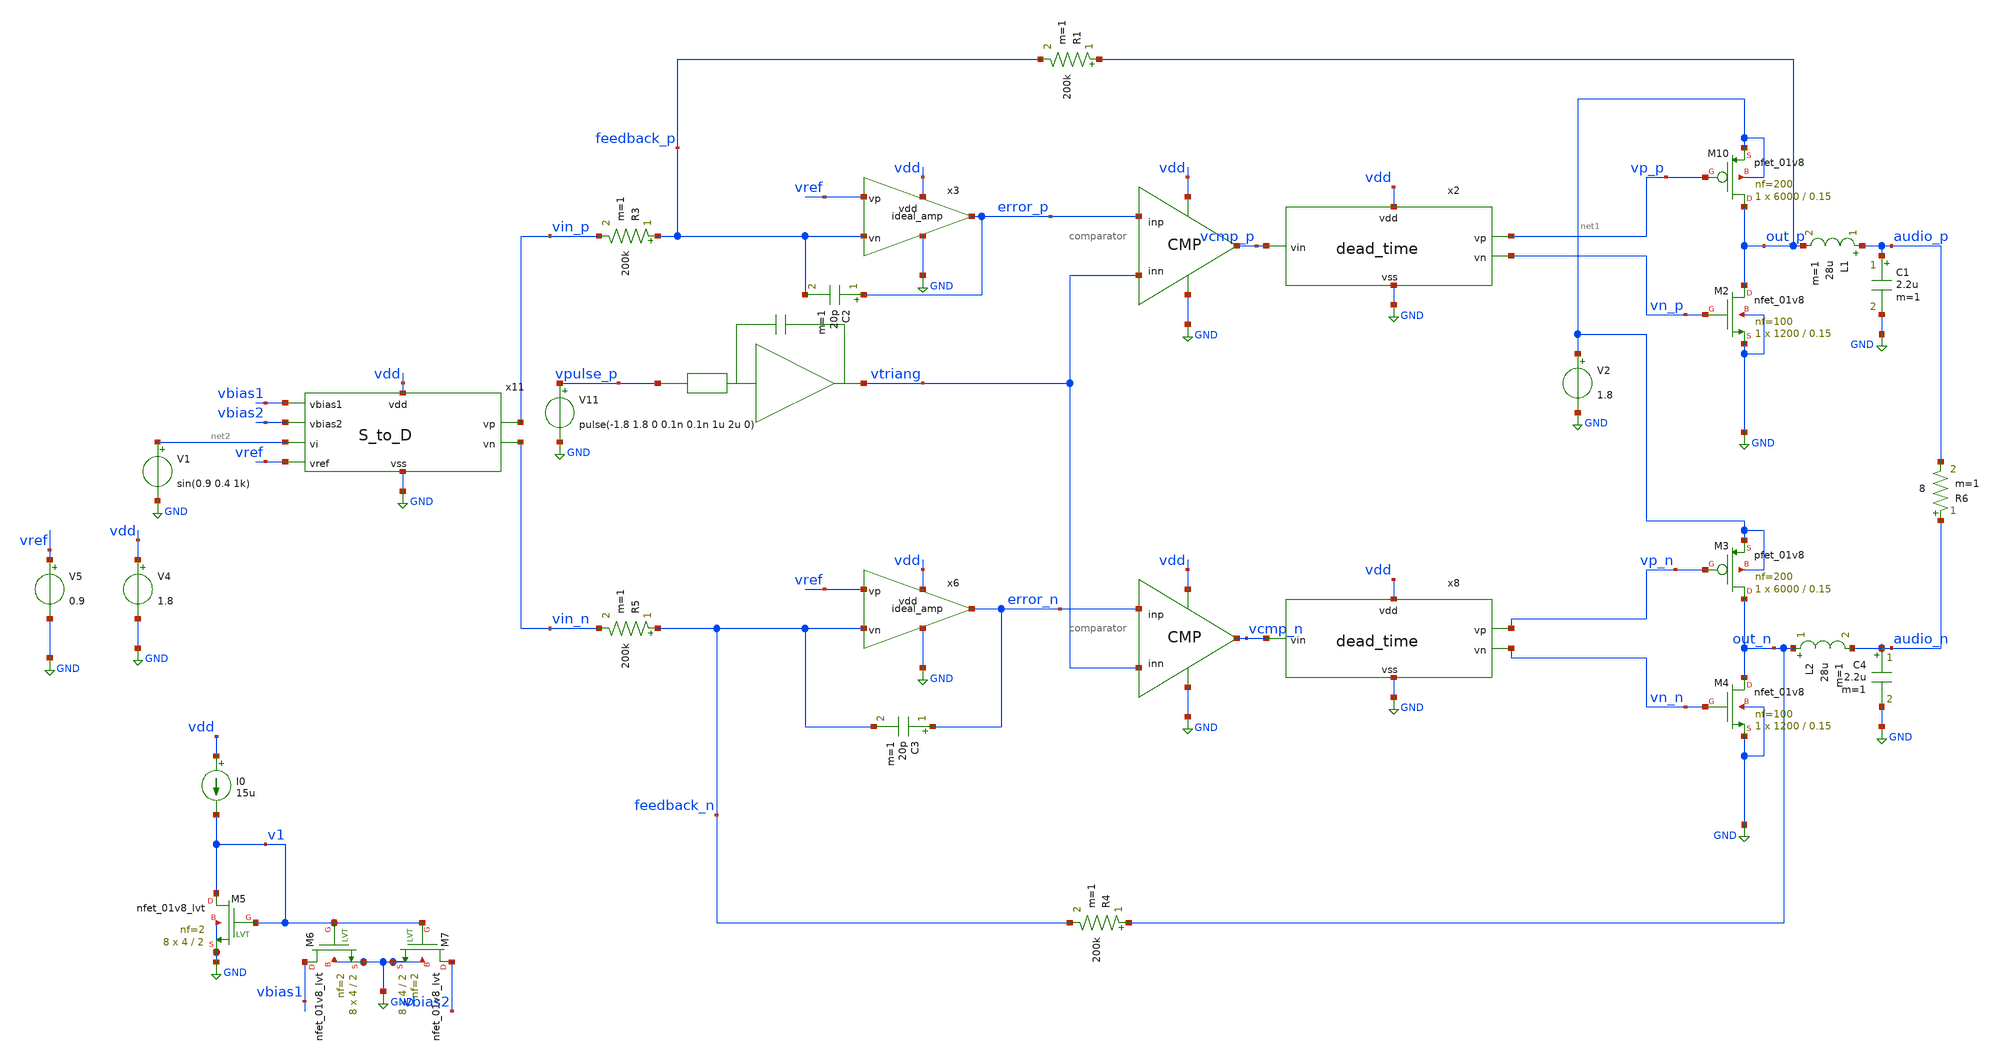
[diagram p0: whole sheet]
** sch_path: xschem/src/behavior_mdl/behavior_model_fine.sch
**.subckt behavior_model_fine
V1 net2 GND sin(0.9 0.4 1k)
x5 vpulse_p vtriang triang
V5 vref GND 0.9
x3 vref feedback_p error_p vdd GND ideal_amp
x1 error_p vtriang vcmp_p vdd GND comparator
L1 audio_p out_p 28u m=1
C1 audio_p GND 2.2u m=1
R1 out_p feedback_p 200k m=1
R3 feedback_p vin_p 200k m=1
C2 error_p feedback_p 20p m=1
x6 vref feedback_n error_n vdd GND ideal_amp
x7 error_n vtriang vcmp_n vdd GND comparator
R4 out_n feedback_n 200k m=1
R5 feedback_n vin_n 200k m=1
C3 error_n feedback_n 20p m=1
L2 out_n audio_n 28u m=1
C4 audio_n GND 2.2u m=1
R6 audio_n audio_p 8 m=1
V11 vpulse_p GND pulse(-1.8 1.8 0 0.1n 0.1n 1u 2u 0)
XM10 out_p vp_p net1 net1 sky130_fd_pr__pfet_01v8 L=0.15 W=6000 nf=200 ad='int((nf+1)/2) * W/nf * 0.29'
+ as='int((nf+2)/2) * W/nf * 0.29' pd='2*int((nf+1)/2) * (W/nf + 0.29)' ps='2*int((nf+2)/2) * (W/nf + 0.29)'
+ nrd='0.29 / W' nrs='0.29 / W' sa=0 sb=0 sd=0 mult=1 m=1
XM2 out_p vn_p GND GND sky130_fd_pr__nfet_01v8 L=0.15 W=1200 nf=100 ad='int((nf+1)/2) * W/nf * 0.29'
+ as='int((nf+2)/2) * W/nf * 0.29' pd='2*int((nf+1)/2) * (W/nf + 0.29)' ps='2*int((nf+2)/2) * (W/nf + 0.29)'
+ nrd='0.29 / W' nrs='0.29 / W' sa=0 sb=0 sd=0 mult=1 m=1
XM3 out_n vp_n net1 net1 sky130_fd_pr__pfet_01v8 L=0.15 W=6000 nf=200 ad='int((nf+1)/2) * W/nf * 0.29'
+ as='int((nf+2)/2) * W/nf * 0.29' pd='2*int((nf+1)/2) * (W/nf + 0.29)' ps='2*int((nf+2)/2) * (W/nf + 0.29)'
+ nrd='0.29 / W' nrs='0.29 / W' sa=0 sb=0 sd=0 mult=1 m=1
XM4 out_n vn_n GND GND sky130_fd_pr__nfet_01v8 L=0.15 W=1200 nf=100 ad='int((nf+1)/2) * W/nf * 0.29'
+ as='int((nf+2)/2) * W/nf * 0.29' pd='2*int((nf+1)/2) * (W/nf + 0.29)' ps='2*int((nf+2)/2) * (W/nf + 0.29)'
+ nrd='0.29 / W' nrs='0.29 / W' sa=0 sb=0 sd=0 mult=1 m=1
V4 vdd GND 1.8
x2 vdd vcmp_p vp_p vn_p GND dead_time
x8 vdd vcmp_n vp_n vn_n GND dead_time
x11 vdd vbias1 vbias2 net2 vref GND vin_n vin_p S_to_D
V2 net1 GND 1.8
I0 vdd v1 15u
XM5 v1 v1 GND GND sky130_fd_pr__nfet_01v8_lvt L=2 W=4 nf=2 ad='int((nf+1)/2) * W/nf * 0.29' as='int((nf+2)/2) * W/nf * 0.29'
+ pd='2*int((nf+1)/2) * (W/nf + 0.29)' ps='2*int((nf+2)/2) * (W/nf + 0.29)' nrd='0.29 / W' nrs='0.29 / W'
+ sa=0 sb=0 sd=0 mult=8 m=8
XM6 vbias1 v1 GND GND sky130_fd_pr__nfet_01v8_lvt L=2 W=4 nf=2 ad='int((nf+1)/2) * W/nf * 0.29' as='int((nf+2)/2) * W/nf * 0.29'
+ pd='2*int((nf+1)/2) * (W/nf + 0.29)' ps='2*int((nf+2)/2) * (W/nf + 0.29)' nrd='0.29 / W' nrs='0.29 / W'
+ sa=0 sb=0 sd=0 mult=8 m=8
XM7 vbias2 v1 GND GND sky130_fd_pr__nfet_01v8_lvt L=2 W=4 nf=2 ad='int((nf+1)/2) * W/nf * 0.29' as='int((nf+2)/2) * W/nf * 0.29'
+ pd='2*int((nf+1)/2) * (W/nf + 0.29)' ps='2*int((nf+2)/2) * (W/nf + 0.29)' nrd='0.29 / W' nrs='0.29 / W'
+ sa=0 sb=0 sd=0 mult=8 m=8
**** begin user architecture code


.include /home/eda/xschem/xschem_library/src/behavior_mdl/comparator.spice
.include /home/eda/xschem/xschem_library/src/behavior_mdl/switch.spice
*.include /home/eda/xschem/xschem_library/src/behavior_mdl/integrator_feedback.spice
*.include /home/eda/xschem/xschem_library/src/behavior_mdl/integrator_input.spice
*.include /home/eda/xschem/xschem_library/src/behavior_mdl/adder.spice
.include /home/eda/xschem/xschem_library/src/behavior_mdl/triang.spice
.include /home/eda/xschem/xschem_library/src/behavior_mdl/ideal_amp.spice
.include /home/eda/xschem/xschem_library/src/behavior_mdl/limiter.spice




.option VNTOL=1e-6 ABSTOL=5e-9
.nodeset v(vin_p)=0.9 v(vin_n)=0.9 v(out_p)=0.9 v(out_n)=0.9 v(error_p)=0.9 v(error_n)=0.9
*set the absolute voltage error tolerance and absolute current error tolerance
.control
save vtriang vin_p vin_n error_n error_p vcmp_n vcmp_p vp_p vn_p vp_n vn_n out_p out_n audio_p
+ audio_n feedback_p feedback_n I(V4) I(V2) @r6[i] @r1[i]
tran 1n 10m 1m
*op
*linearize V(audio)
*linearize V(out)
*fft V(out)
*fft V(audio)
*plot mag(V(audio))
*plot mag(V(out))
let pout=@r6[i]*(V(audio_p)-V(audio_n))
let pin=1.8*I(V2)
meas tran pload avg pout from=1m to=4m
meas tran p_supply avg pin from=1m to=4m
print pload/p_supply
set nfreqs=20
fourier 1k V(audio_p)-V(audio_n)
write behavior_1k_04.raw

.endc





.include /home/eda/pdk/skywater-pdk/libraries/sky130_fd_pr_ngspice/latest/models/corners/tt.spice
.include /home/eda/magic/class_d_audio_amplifier/OTA/OTA_int_post.spice
.include /home/eda/magic/class_d_audio_amplifier/OTA/OTA_post.spice
.include /home/eda/magic/class_d_audio_amplifier/S_to_D/S_to_D_post.spice
.include /home/eda/magic/class_d_audio_amplifier/triang/triangle_post.spice

* Resistor$::SKYWATER_MODELS/Capacitor
.include $::SKYWATER_MODELS/models/r+c/res_typical__cap_typical.spice
.include $::SKYWATER_MODELS/models/r+c/res_typical__cap_typical__lin.spice
* Special cells
.include $::SKYWATER_MODELS/models/corners/tt/specialized_cells.spice


**** end user architecture code
**.ends

* expanding   symbol:  src/dead_time/dead_time.sym # of pins=5
** sym_path: xschem/src/dead_time/dead_time.sym
** sch_path: xschem/src/dead_time/dead_time.sch
.subckt dead_time vdd vin vp vn vss
*.ipin vin
*.iopin vdd
*.opin vp
*.iopin vss
*.opin vn
x1 vdd vin vinn vss inverter
x2 vdd net1 vin net4 vss nand
x3 vdd net2 net3 vinn vss nand
XC1 net1 vss sky130_fd_pr__cap_mim_m3_1 W=17.75 L=17.75 MF=16 m=16
XM3 net5 net1 vss vss sky130_fd_pr__nfet_01v8 L=0.15 W=5 nf=2 ad='int((nf+1)/2) * W/nf * 0.29' as='int((nf+2)/2) * W/nf * 0.29'
+ pd='2*int((nf+1)/2) * (W/nf + 0.29)' ps='2*int((nf+2)/2) * (W/nf + 0.29)' nrd='0.29 / W' nrs='0.29 / W'
+ sa=0 sb=0 sd=0 mult=1 m=1
XM1 net5 net1 vdd vdd sky130_fd_pr__pfet_01v8 L=0.15 W=10 nf=2 ad='int((nf+1)/2) * W/nf * 0.29' as='int((nf+2)/2) * W/nf * 0.29'
+ pd='2*int((nf+1)/2) * (W/nf + 0.29)' ps='2*int((nf+2)/2) * (W/nf + 0.29)' nrd='0.29 / W' nrs='0.29 / W'
+ sa=0 sb=0 sd=0 mult=1 m=1
XM2 net3 net5 vss vss sky130_fd_pr__nfet_01v8 L=0.15 W=20 nf=8 ad='int((nf+1)/2) * W/nf * 0.29' as='int((nf+2)/2) * W/nf * 0.29'
+ pd='2*int((nf+1)/2) * (W/nf + 0.29)' ps='2*int((nf+2)/2) * (W/nf + 0.29)' nrd='0.29 / W' nrs='0.29 / W'
+ sa=0 sb=0 sd=0 mult=1 m=1
XM4 net3 net5 vdd vdd sky130_fd_pr__pfet_01v8 L=0.15 W=40 nf=8 ad='int((nf+1)/2) * W/nf * 0.29' as='int((nf+2)/2) * W/nf * 0.29'
+ pd='2*int((nf+1)/2) * (W/nf + 0.29)' ps='2*int((nf+2)/2) * (W/nf + 0.29)' nrd='0.29 / W' nrs='0.29 / W'
+ sa=0 sb=0 sd=0 mult=1 m=1
XM5 net6 net3 vss vss sky130_fd_pr__nfet_01v8 L=0.15 W=90 nf=36 ad='int((nf+1)/2) * W/nf * 0.29' as='int((nf+2)/2) * W/nf * 0.29'
+ pd='2*int((nf+1)/2) * (W/nf + 0.29)' ps='2*int((nf+2)/2) * (W/nf + 0.29)' nrd='0.29 / W' nrs='0.29 / W'
+ sa=0 sb=0 sd=0 mult=1 m=1
XM6 net6 net3 vdd vdd sky130_fd_pr__pfet_01v8 L=0.15 W=180 nf=36 ad='int((nf+1)/2) * W/nf * 0.29' as='int((nf+2)/2) * W/nf * 0.29'
+ pd='2*int((nf+1)/2) * (W/nf + 0.29)' ps='2*int((nf+2)/2) * (W/nf + 0.29)' nrd='0.29 / W' nrs='0.29 / W'
+ sa=0 sb=0 sd=0 mult=1 m=1
XM7 vp net6 vss vss sky130_fd_pr__nfet_01v8 L=0.15 W=200 nf=81 ad='int((nf+1)/2) * W/nf * 0.29' as='int((nf+2)/2) * W/nf * 0.29'
+ pd='2*int((nf+1)/2) * (W/nf + 0.29)' ps='2*int((nf+2)/2) * (W/nf + 0.29)' nrd='0.29 / W' nrs='0.29 / W'
+ sa=0 sb=0 sd=0 mult=2 m=2
XM8 vp net6 vdd vdd sky130_fd_pr__pfet_01v8 L=0.15 W=400 nf=81 ad='int((nf+1)/2) * W/nf * 0.29' as='int((nf+2)/2) * W/nf * 0.29'
+ pd='2*int((nf+1)/2) * (W/nf + 0.29)' ps='2*int((nf+2)/2) * (W/nf + 0.29)' nrd='0.29 / W' nrs='0.29 / W'
+ sa=0 sb=0 sd=0 mult=2 m=2
XM9 net7 net2 vss vss sky130_fd_pr__nfet_01v8 L=0.15 W=5 nf=2 ad='int((nf+1)/2) * W/nf * 0.29' as='int((nf+2)/2) * W/nf * 0.29'
+ pd='2*int((nf+1)/2) * (W/nf + 0.29)' ps='2*int((nf+2)/2) * (W/nf + 0.29)' nrd='0.29 / W' nrs='0.29 / W'
+ sa=0 sb=0 sd=0 mult=1 m=1
XM10 net7 net2 vdd vdd sky130_fd_pr__pfet_01v8 L=0.15 W=10 nf=2 ad='int((nf+1)/2) * W/nf * 0.29' as='int((nf+2)/2) * W/nf * 0.29'
+ pd='2*int((nf+1)/2) * (W/nf + 0.29)' ps='2*int((nf+2)/2) * (W/nf + 0.29)' nrd='0.29 / W' nrs='0.29 / W'
+ sa=0 sb=0 sd=0 mult=1 m=1
XM11 net4 net7 vss vss sky130_fd_pr__nfet_01v8 L=0.15 W=20 nf=8 ad='int((nf+1)/2) * W/nf * 0.29' as='int((nf+2)/2) * W/nf * 0.29'
+ pd='2*int((nf+1)/2) * (W/nf + 0.29)' ps='2*int((nf+2)/2) * (W/nf + 0.29)' nrd='0.29 / W' nrs='0.29 / W'
+ sa=0 sb=0 sd=0 mult=1 m=1
XM12 net4 net7 vdd vdd sky130_fd_pr__pfet_01v8 L=0.15 W=40 nf=8 ad='int((nf+1)/2) * W/nf * 0.29' as='int((nf+2)/2) * W/nf * 0.29'
+ pd='2*int((nf+1)/2) * (W/nf + 0.29)' ps='2*int((nf+2)/2) * (W/nf + 0.29)' nrd='0.29 / W' nrs='0.29 / W'
+ sa=0 sb=0 sd=0 mult=1 m=1
XM13 vn net4 vss vss sky130_fd_pr__nfet_01v8 L=0.15 W=90 nf=36 ad='int((nf+1)/2) * W/nf * 0.29' as='int((nf+2)/2) * W/nf * 0.29'
+ pd='2*int((nf+1)/2) * (W/nf + 0.29)' ps='2*int((nf+2)/2) * (W/nf + 0.29)' nrd='0.29 / W' nrs='0.29 / W'
+ sa=0 sb=0 sd=0 mult=1 m=1
XM14 vn net4 vdd vdd sky130_fd_pr__pfet_01v8 L=0.15 W=180 nf=36 ad='int((nf+1)/2) * W/nf * 0.29' as='int((nf+2)/2) * W/nf * 0.29'
+ pd='2*int((nf+1)/2) * (W/nf + 0.29)' ps='2*int((nf+2)/2) * (W/nf + 0.29)' nrd='0.29 / W' nrs='0.29 / W'
+ sa=0 sb=0 sd=0 mult=1 m=1
XC2 net2 vss sky130_fd_pr__cap_mim_m3_1 W=17.75 L=17.75 MF=16 m=16
.ends


* expanding   symbol:  src/S_to_D/S_to_D.sym # of pins=8
** sym_path: xschem/src/S_to_D/S_to_D.sym
** sch_path: xschem/src/S_to_D/S_to_D.sch
.subckt S_to_D vdd vbias1 vbias2 vi vref vss vn vp
*.iopin vdd
*.iopin vss
*.ipin vi
*.opin vp
*.opin vn
*.ipin vref
*.ipin vbias1
*.ipin vbias2
x1 vdd vref v1 vbias2 vss vn OTA
XR2 vn v1 vss sky130_fd_pr__res_xhigh_po L=10 mult=1 m=1
x2 vdd vi vp vbias1 vss vp OTA
XR1 v1 vi vss sky130_fd_pr__res_xhigh_po L=10 mult=1 m=1
.ends


* expanding   symbol:  src/inverter/inverter.sym # of pins=4
** sym_path: xschem/src/inverter/inverter.sym
** sch_path: xschem/src/inverter/inverter.sch
.subckt inverter vdd A B vss
*.iopin vdd
*.iopin vss
*.ipin A
*.opin B
XM3 B A vss vss sky130_fd_pr__nfet_01v8 L=0.15 W=1 nf=1 ad='int((nf+1)/2) * W/nf * 0.29' as='int((nf+2)/2) * W/nf * 0.29'
+ pd='2*int((nf+1)/2) * (W/nf + 0.29)' ps='2*int((nf+2)/2) * (W/nf + 0.29)' nrd='0.29 / W' nrs='0.29 / W'
+ sa=0 sb=0 sd=0 mult=1 m=1
XM1 B A vdd vdd sky130_fd_pr__pfet_01v8 L=0.15 W=2 nf=1 ad='int((nf+1)/2) * W/nf * 0.29' as='int((nf+2)/2) * W/nf * 0.29'
+ pd='2*int((nf+1)/2) * (W/nf + 0.29)' ps='2*int((nf+2)/2) * (W/nf + 0.29)' nrd='0.29 / W' nrs='0.29 / W'
+ sa=0 sb=0 sd=0 mult=1 m=1
.ends


* expanding   symbol:  src/nand/nand.sym # of pins=5
** sym_path: xschem/src/nand/nand.sym
** sch_path: xschem/src/nand/nand.sch
.subckt nand vdd out A B vss
*.ipin A
*.ipin B
*.opin out
*.iopin vdd
*.iopin vss
XM1 out A net1 vss sky130_fd_pr__nfet_01v8 L=0.15 W=2 nf=1 ad='int((nf+1)/2) * W/nf * 0.29' as='int((nf+2)/2) * W/nf * 0.29'
+ pd='2*int((nf+1)/2) * (W/nf + 0.29)' ps='2*int((nf+2)/2) * (W/nf + 0.29)' nrd='0.29 / W' nrs='0.29 / W'
+ sa=0 sb=0 sd=0 mult=1 m=1
XM2 out A vdd vdd sky130_fd_pr__pfet_01v8 L=0.15 W=2 nf=1 ad='int((nf+1)/2) * W/nf * 0.29' as='int((nf+2)/2) * W/nf * 0.29'
+ pd='2*int((nf+1)/2) * (W/nf + 0.29)' ps='2*int((nf+2)/2) * (W/nf + 0.29)' nrd='0.29 / W' nrs='0.29 / W'
+ sa=0 sb=0 sd=0 mult=1 m=1
XM3 net1 B vss vss sky130_fd_pr__nfet_01v8 L=0.15 W=2 nf=1 ad='int((nf+1)/2) * W/nf * 0.29' as='int((nf+2)/2) * W/nf * 0.29'
+ pd='2*int((nf+1)/2) * (W/nf + 0.29)' ps='2*int((nf+2)/2) * (W/nf + 0.29)' nrd='0.29 / W' nrs='0.29 / W'
+ sa=0 sb=0 sd=0 mult=1 m=1
XM4 out B vdd vdd sky130_fd_pr__pfet_01v8 L=0.15 W=2 nf=1 ad='int((nf+1)/2) * W/nf * 0.29' as='int((nf+2)/2) * W/nf * 0.29'
+ pd='2*int((nf+1)/2) * (W/nf + 0.29)' ps='2*int((nf+2)/2) * (W/nf + 0.29)' nrd='0.29 / W' nrs='0.29 / W'
+ sa=0 sb=0 sd=0 mult=1 m=1
.ends


* expanding   symbol:  src/OTA/OTA.sym # of pins=6
** sym_path: xschem/src/OTA/OTA.sym
** sch_path: xschem/src/OTA/OTA.sch
.subckt OTA vdd vp vn vbias vss vout
*.ipin vp
*.ipin vn
*.ipin vbias
*.iopin vss
*.iopin vdd
*.opin vout
XM1 v1 vp vc vc sky130_fd_pr__pfet_01v8_lvt L=1 W=4 nf=1 ad='int((nf+1)/2) * W/nf * 0.29' as='int((nf+2)/2) * W/nf * 0.29'
+ pd='2*int((nf+1)/2) * (W/nf + 0.29)' ps='2*int((nf+2)/2) * (W/nf + 0.29)' nrd='0.29 / W' nrs='0.29 / W'
+ sa=0 sb=0 sd=0 mult=16 m=16
XM2 vf vn vc vc sky130_fd_pr__pfet_01v8_lvt L=1 W=4 nf=1 ad='int((nf+1)/2) * W/nf * 0.29' as='int((nf+2)/2) * W/nf * 0.29'
+ pd='2*int((nf+1)/2) * (W/nf + 0.29)' ps='2*int((nf+2)/2) * (W/nf + 0.29)' nrd='0.29 / W' nrs='0.29 / W'
+ sa=0 sb=0 sd=0 mult=16 m=16
XM3 vc vbias vdd vdd sky130_fd_pr__pfet_01v8_lvt L=1 W=2 nf=2 ad='int((nf+1)/2) * W/nf * 0.29' as='int((nf+2)/2) * W/nf * 0.29'
+ pd='2*int((nf+1)/2) * (W/nf + 0.29)' ps='2*int((nf+2)/2) * (W/nf + 0.29)' nrd='0.29 / W' nrs='0.29 / W'
+ sa=0 sb=0 sd=0 mult=24 m=24
XM4 v1 vf vss vss sky130_fd_pr__nfet_01v8_lvt L=1 W=1 nf=1 ad='int((nf+1)/2) * W/nf * 0.29' as='int((nf+2)/2) * W/nf * 0.29'
+ pd='2*int((nf+1)/2) * (W/nf + 0.29)' ps='2*int((nf+2)/2) * (W/nf + 0.29)' nrd='0.29 / W' nrs='0.29 / W'
+ sa=0 sb=0 sd=0 mult=16 m=16
XM5 vf vf vss vss sky130_fd_pr__nfet_01v8_lvt L=1 W=1 nf=1 ad='int((nf+1)/2) * W/nf * 0.29' as='int((nf+2)/2) * W/nf * 0.29'
+ pd='2*int((nf+1)/2) * (W/nf + 0.29)' ps='2*int((nf+2)/2) * (W/nf + 0.29)' nrd='0.29 / W' nrs='0.29 / W'
+ sa=0 sb=0 sd=0 mult=16 m=16
XM6 vbias vbias vdd vdd sky130_fd_pr__pfet_01v8_lvt L=1 W=2 nf=2 ad='int((nf+1)/2) * W/nf * 0.29' as='int((nf+2)/2) * W/nf * 0.29'
+ pd='2*int((nf+1)/2) * (W/nf + 0.29)' ps='2*int((nf+2)/2) * (W/nf + 0.29)' nrd='0.29 / W' nrs='0.29 / W'
+ sa=0 sb=0 sd=0 mult=24 m=24
XM7 vout vbias vdd vdd sky130_fd_pr__pfet_01v8_lvt L=1 W=2 nf=2 ad='int((nf+1)/2) * W/nf * 0.29' as='int((nf+2)/2) * W/nf * 0.29'
+ pd='2*int((nf+1)/2) * (W/nf + 0.29)' ps='2*int((nf+2)/2) * (W/nf + 0.29)' nrd='0.29 / W' nrs='0.29 / W'
+ sa=0 sb=0 sd=0 mult=48 m=48
XM8 vout v1 vss vss sky130_fd_pr__nfet_01v8_lvt L=1 W=1 nf=1 ad='int((nf+1)/2) * W/nf * 0.29' as='int((nf+2)/2) * W/nf * 0.29'
+ pd='2*int((nf+1)/2) * (W/nf + 0.29)' ps='2*int((nf+2)/2) * (W/nf + 0.29)' nrd='0.29 / W' nrs='0.29 / W'
+ sa=0 sb=0 sd=0 mult=64 m=64
XR1 v1 net1 vss sky130_fd_pr__res_xhigh_po W=0.35 L=0.5 mult=1 m=1
XC2 net1 vout sky130_fd_pr__cap_mim_m3_1 W=14 L=14 MF=1 m=1
.ends

.GLOBAL GND
.end
